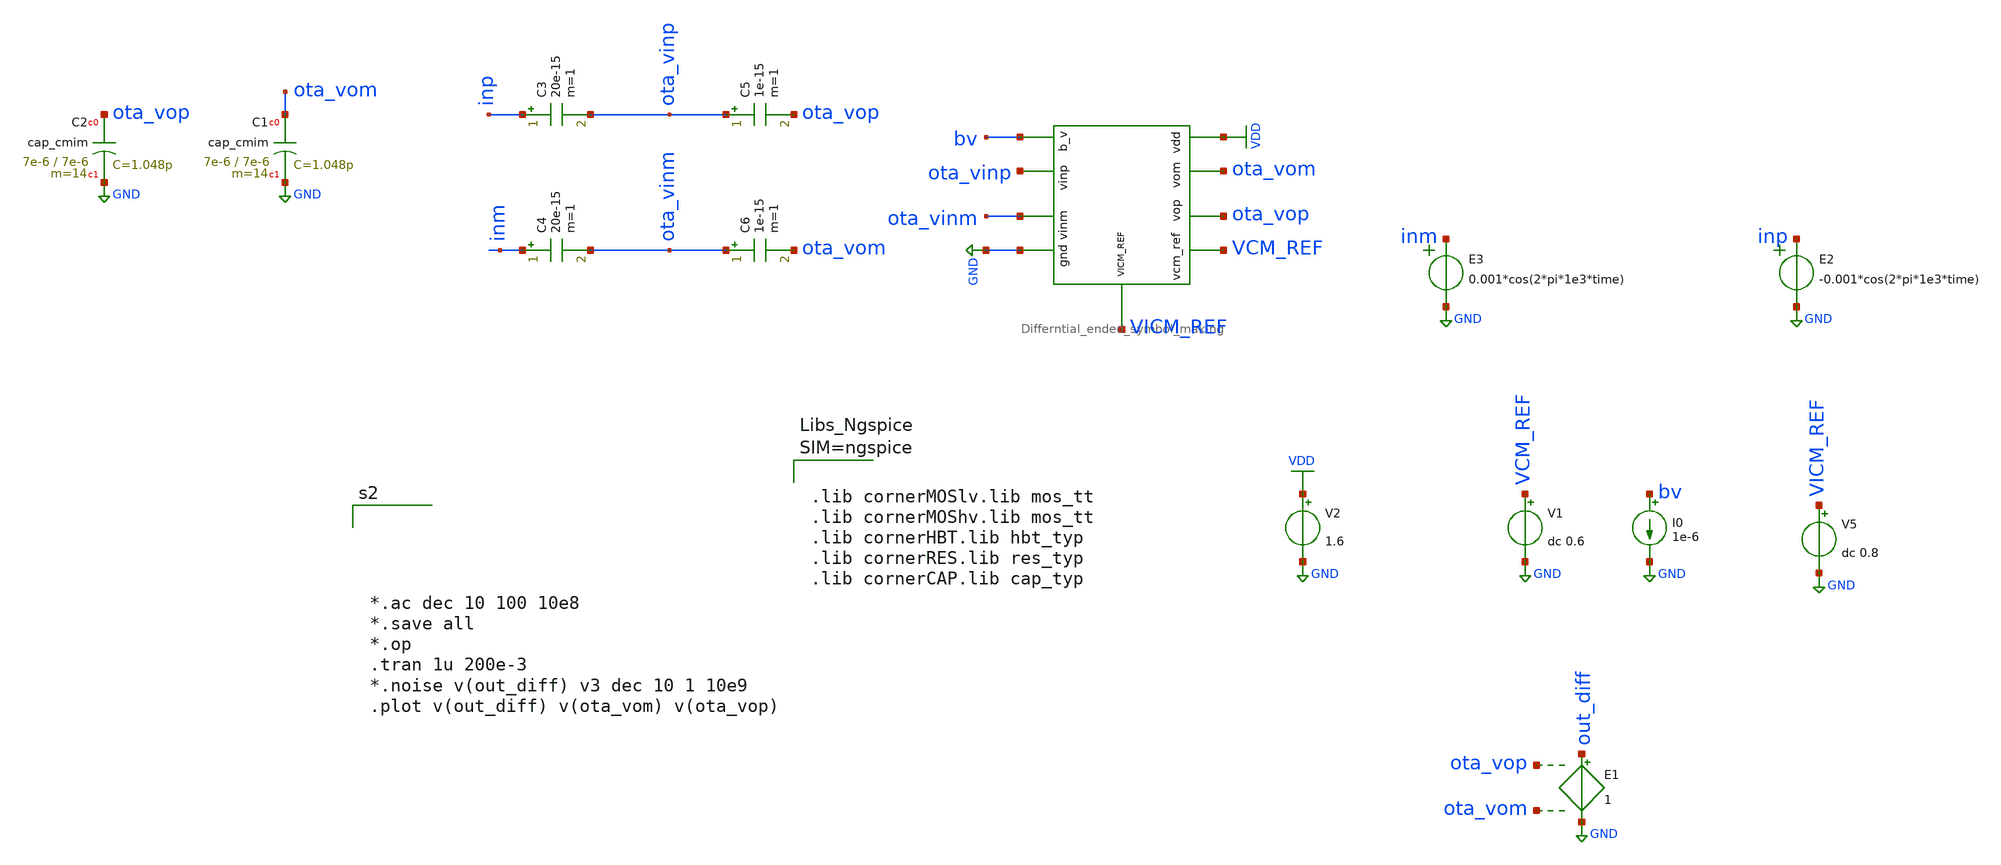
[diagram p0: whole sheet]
** sch_path: dependencies/OTA/OTA-main/testbenches/tb_ota_closed_loop.sch
**.subckt tb_ota_closed_loop
V2 VDD GND 1.6
V1 VCM_REF GND dc 0.6
I0 bv GND 1e-6
V5 VICM_REF GND dc 0.8
E1 out_diff GND ota_vop ota_vom 1
x1 VDD VCM_REF ota_vom ota_vop GND bv ota_vinm ota_vinp VICM_REF Differntial_ended_symbol_making
E3 inm GND VOL=' 0.001*cos(2*pi*1e3*time) '
XC1 ota_vom GND cap_cmim w=7e-6 l=7e-6 m=14 mm_ok=1
XC2 ota_vop GND cap_cmim w=7e-6 l=7e-6 m=14 mm_ok=1
E2 inp GND VOL=' -0.001*cos(2*pi*1e3*time) '
C3 inp ota_vinp 20e-15 m=1
C4 inm ota_vinm 20e-15 m=1
C5 ota_vinp ota_vop 1e-15 m=1
C6 ota_vinm ota_vom 1e-15 m=1
**** begin user architecture code



.lib cornerMOSlv.lib mos_tt
.lib cornerMOShv.lib mos_tt
.lib cornerHBT.lib hbt_typ
.lib cornerRES.lib res_typ
.lib cornerCAP.lib cap_typ








*.ac dec 10 100 10e8
*.save all
*.op
.tran 1u 200e-3
*.noise v(out_diff) v3 dec 10 1 10e9
.plot v(out_diff) v(ota_vom) v(ota_vop)




**** end user architecture code
**.ends

* expanding   symbol:
*+  /home/designer/shared/unicass_2026/Design_Files/github_clone_circuit_/UNI-CASS_Project_2025_IIT_DH/Differntial_ended_symbol_making.sym # of pins=9
** sym_path: /home/designer/shared/unicass_2026/Design_Files/github_clone_circuit_/UNI-CASS_Project_2025_IIT_DH/Differntial_ended_symbol_making.sym
** sch_path: /home/designer/shared/unicass_2026/Design_Files/github_clone_circuit_/UNI-CASS_Project_2025_IIT_DH/Differntial_ended_symbol_making.sch
.subckt Differntial_ended_symbol_making vdd vcm_ref vom vop gnd b_v vinm vinp VICM_REF
*.iopin b_v
*.iopin vinm
*.iopin vcm_ref
*.iopin vinp
*.iopin vop
*.iopin vom
*.iopin gnd
*.iopin vdd
*.iopin VICM_REF
XM7 vop nbias gnd gnd sg13_hv_nmos w=2u l=2u ng=1 m=2 mm_ok=1
XM8 vop vinm tail vdd sg13_hv_pmos w=4.5u l=1u ng=1 m=2 mm_ok=1
XM9 vom nbias gnd gnd sg13_hv_nmos w=2u l=2u ng=1 m=2 mm_ok=1
XM10 vom vinp tail vdd sg13_hv_pmos w=4.5u l=1u ng=1 m=2 mm_ok=1
XM11 tail b_v vdd vdd sg13_hv_pmos w=4u l=1u ng=1 m=4 mm_ok=1
XM6 net1 net1 gnd gnd sg13_hv_nmos w=1u l=0.5u ng=1 m=1 mm_ok=1
XM13 net1 vop tail_cmfb vdd sg13_hv_pmos w=2.25u l=0.50u ng=1 m=1 mm_ok=1
XM14 nbias net1 gnd gnd sg13_hv_nmos w=1u l=0.5u ng=1 m=1 mm_ok=1
XM15 nbias vcm_ref tail_cmfb vdd sg13_hv_pmos w=2.25u l=0.5u ng=1 m=2 mm_ok=1
XM16 tail_cmfb b_v vdd vdd sg13_hv_pmos w=4u l=1u ng=1 m=4 mm_ok=1
XM17 net1 vom tail_cmfb vdd sg13_hv_pmos w=2.25u l=0.50u ng=1 m=1 mm_ok=1
XM1 b_v b_v vdd vdd sg13_hv_pmos w=4u l=1u ng=1 m=1 mm_ok=1
XC1 nbias gnd cap_cmim w=14.0e-6 l=50.0e-6 m=1 mm_ok=1
XM2 VICM_REF vinm vinm vdd sg13_hv_pmos w=50u l=1u ng=5 m=1 mm_ok=1
XM3 VICM_REF vinp vinp vdd sg13_hv_pmos w=50u l=1u ng=5 m=1 mm_ok=1
XM4 vdd vdd vdd vdd sg13_hv_pmos w=4.5u l=0.4u ng=1 m=4 mm_ok=1
XM5 gnd gnd gnd gnd sg13_hv_nmos w=2u l=2u ng=1 m=4 mm_ok=1
.ends

.GLOBAL GND
.GLOBAL VDD
.end
